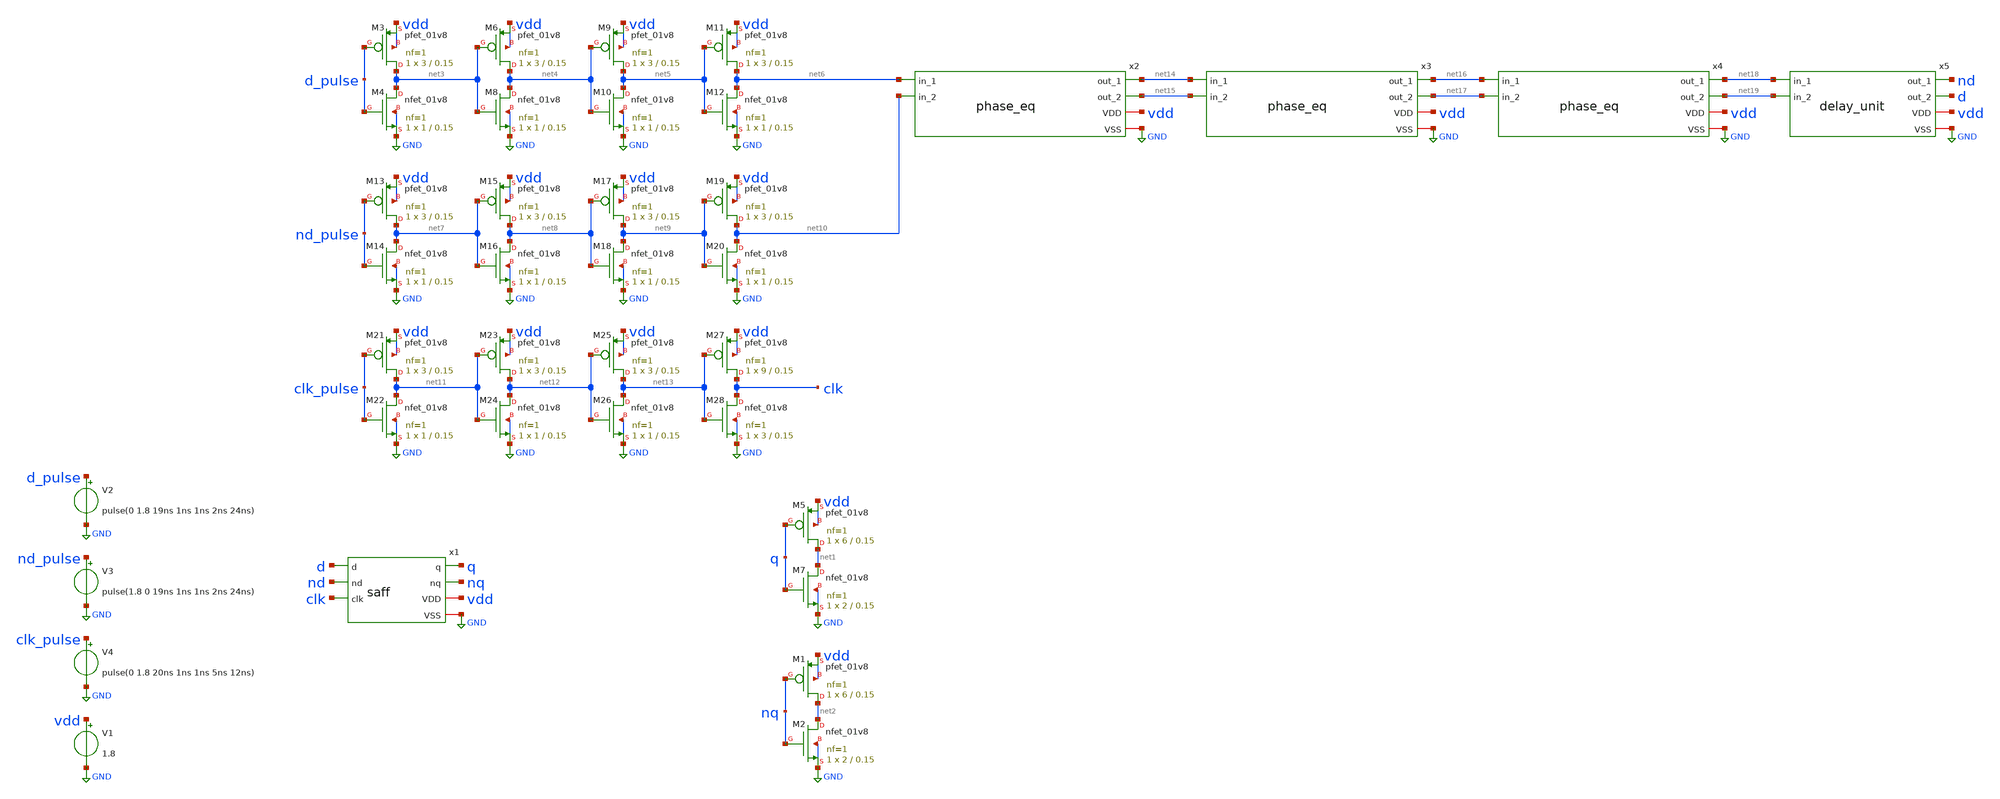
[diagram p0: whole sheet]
** sch_path: xschem/saff_tb.sch
**.subckt saff_tb
x1 d nd clk q nq vdd GND saff
V1 vdd GND 1.8
V2 d_pulse GND pulse(0 1.8 19ns 1ns 1ns 2ns 24ns)
V3 nd_pulse GND pulse(1.8 0 19ns 1ns 1ns 2ns 24ns)
V4 clk_pulse GND pulse(0 1.8 20ns 1ns 1ns 5ns 12ns)
XM5 net1 q vdd vdd sky130_fd_pr__pfet_01v8 L=0.15 W=6 nf=1 ad='int((nf+1)/2) * W/nf * 0.29' as='int((nf+2)/2) * W/nf * 0.29'
+ pd='2*int((nf+1)/2) * (W/nf + 0.29)' ps='2*int((nf+2)/2) * (W/nf + 0.29)' nrd='0.29 / W' nrs='0.29 / W'
+ sa=0 sb=0 sd=0 mult=1 m=1
XM7 net1 q GND GND sky130_fd_pr__nfet_01v8 L=0.15 W=2 nf=1 ad='int((nf+1)/2) * W/nf * 0.29' as='int((nf+2)/2) * W/nf * 0.29'
+ pd='2*int((nf+1)/2) * (W/nf + 0.29)' ps='2*int((nf+2)/2) * (W/nf + 0.29)' nrd='0.29 / W' nrs='0.29 / W'
+ sa=0 sb=0 sd=0 mult=1 m=1
XM1 net2 nq vdd vdd sky130_fd_pr__pfet_01v8 L=0.15 W=6 nf=1 ad='int((nf+1)/2) * W/nf * 0.29' as='int((nf+2)/2) * W/nf * 0.29'
+ pd='2*int((nf+1)/2) * (W/nf + 0.29)' ps='2*int((nf+2)/2) * (W/nf + 0.29)' nrd='0.29 / W' nrs='0.29 / W'
+ sa=0 sb=0 sd=0 mult=1 m=1
XM2 net2 nq GND GND sky130_fd_pr__nfet_01v8 L=0.15 W=2 nf=1 ad='int((nf+1)/2) * W/nf * 0.29' as='int((nf+2)/2) * W/nf * 0.29'
+ pd='2*int((nf+1)/2) * (W/nf + 0.29)' ps='2*int((nf+2)/2) * (W/nf + 0.29)' nrd='0.29 / W' nrs='0.29 / W'
+ sa=0 sb=0 sd=0 mult=1 m=1
XM3 net3 d_pulse vdd vdd sky130_fd_pr__pfet_01v8 L=0.15 W=3 nf=1 ad='int((nf+1)/2) * W/nf * 0.29' as='int((nf+2)/2) * W/nf * 0.29'
+ pd='2*int((nf+1)/2) * (W/nf + 0.29)' ps='2*int((nf+2)/2) * (W/nf + 0.29)' nrd='0.29 / W' nrs='0.29 / W'
+ sa=0 sb=0 sd=0 mult=1 m=1
XM4 net3 d_pulse GND GND sky130_fd_pr__nfet_01v8 L=0.15 W=1 nf=1 ad='int((nf+1)/2) * W/nf * 0.29' as='int((nf+2)/2) * W/nf * 0.29'
+ pd='2*int((nf+1)/2) * (W/nf + 0.29)' ps='2*int((nf+2)/2) * (W/nf + 0.29)' nrd='0.29 / W' nrs='0.29 / W'
+ sa=0 sb=0 sd=0 mult=1 m=1
XM6 net4 net3 vdd vdd sky130_fd_pr__pfet_01v8 L=0.15 W=3 nf=1 ad='int((nf+1)/2) * W/nf * 0.29' as='int((nf+2)/2) * W/nf * 0.29'
+ pd='2*int((nf+1)/2) * (W/nf + 0.29)' ps='2*int((nf+2)/2) * (W/nf + 0.29)' nrd='0.29 / W' nrs='0.29 / W'
+ sa=0 sb=0 sd=0 mult=1 m=1
XM8 net4 net3 GND GND sky130_fd_pr__nfet_01v8 L=0.15 W=1 nf=1 ad='int((nf+1)/2) * W/nf * 0.29' as='int((nf+2)/2) * W/nf * 0.29'
+ pd='2*int((nf+1)/2) * (W/nf + 0.29)' ps='2*int((nf+2)/2) * (W/nf + 0.29)' nrd='0.29 / W' nrs='0.29 / W'
+ sa=0 sb=0 sd=0 mult=1 m=1
XM9 net5 net4 vdd vdd sky130_fd_pr__pfet_01v8 L=0.15 W=3 nf=1 ad='int((nf+1)/2) * W/nf * 0.29' as='int((nf+2)/2) * W/nf * 0.29'
+ pd='2*int((nf+1)/2) * (W/nf + 0.29)' ps='2*int((nf+2)/2) * (W/nf + 0.29)' nrd='0.29 / W' nrs='0.29 / W'
+ sa=0 sb=0 sd=0 mult=1 m=1
XM10 net5 net4 GND GND sky130_fd_pr__nfet_01v8 L=0.15 W=1 nf=1 ad='int((nf+1)/2) * W/nf * 0.29' as='int((nf+2)/2) * W/nf * 0.29'
+ pd='2*int((nf+1)/2) * (W/nf + 0.29)' ps='2*int((nf+2)/2) * (W/nf + 0.29)' nrd='0.29 / W' nrs='0.29 / W'
+ sa=0 sb=0 sd=0 mult=1 m=1
XM11 net6 net5 vdd vdd sky130_fd_pr__pfet_01v8 L=0.15 W=3 nf=1 ad='int((nf+1)/2) * W/nf * 0.29' as='int((nf+2)/2) * W/nf * 0.29'
+ pd='2*int((nf+1)/2) * (W/nf + 0.29)' ps='2*int((nf+2)/2) * (W/nf + 0.29)' nrd='0.29 / W' nrs='0.29 / W'
+ sa=0 sb=0 sd=0 mult=1 m=1
XM12 net6 net5 GND GND sky130_fd_pr__nfet_01v8 L=0.15 W=1 nf=1 ad='int((nf+1)/2) * W/nf * 0.29' as='int((nf+2)/2) * W/nf * 0.29'
+ pd='2*int((nf+1)/2) * (W/nf + 0.29)' ps='2*int((nf+2)/2) * (W/nf + 0.29)' nrd='0.29 / W' nrs='0.29 / W'
+ sa=0 sb=0 sd=0 mult=1 m=1
XM13 net7 nd_pulse vdd vdd sky130_fd_pr__pfet_01v8 L=0.15 W=3 nf=1 ad='int((nf+1)/2) * W/nf * 0.29' as='int((nf+2)/2) * W/nf * 0.29'
+ pd='2*int((nf+1)/2) * (W/nf + 0.29)' ps='2*int((nf+2)/2) * (W/nf + 0.29)' nrd='0.29 / W' nrs='0.29 / W'
+ sa=0 sb=0 sd=0 mult=1 m=1
XM14 net7 nd_pulse GND GND sky130_fd_pr__nfet_01v8 L=0.15 W=1 nf=1 ad='int((nf+1)/2) * W/nf * 0.29' as='int((nf+2)/2) * W/nf * 0.29'
+ pd='2*int((nf+1)/2) * (W/nf + 0.29)' ps='2*int((nf+2)/2) * (W/nf + 0.29)' nrd='0.29 / W' nrs='0.29 / W'
+ sa=0 sb=0 sd=0 mult=1 m=1
XM15 net8 net7 vdd vdd sky130_fd_pr__pfet_01v8 L=0.15 W=3 nf=1 ad='int((nf+1)/2) * W/nf * 0.29' as='int((nf+2)/2) * W/nf * 0.29'
+ pd='2*int((nf+1)/2) * (W/nf + 0.29)' ps='2*int((nf+2)/2) * (W/nf + 0.29)' nrd='0.29 / W' nrs='0.29 / W'
+ sa=0 sb=0 sd=0 mult=1 m=1
XM16 net8 net7 GND GND sky130_fd_pr__nfet_01v8 L=0.15 W=1 nf=1 ad='int((nf+1)/2) * W/nf * 0.29' as='int((nf+2)/2) * W/nf * 0.29'
+ pd='2*int((nf+1)/2) * (W/nf + 0.29)' ps='2*int((nf+2)/2) * (W/nf + 0.29)' nrd='0.29 / W' nrs='0.29 / W'
+ sa=0 sb=0 sd=0 mult=1 m=1
XM17 net9 net8 vdd vdd sky130_fd_pr__pfet_01v8 L=0.15 W=3 nf=1 ad='int((nf+1)/2) * W/nf * 0.29' as='int((nf+2)/2) * W/nf * 0.29'
+ pd='2*int((nf+1)/2) * (W/nf + 0.29)' ps='2*int((nf+2)/2) * (W/nf + 0.29)' nrd='0.29 / W' nrs='0.29 / W'
+ sa=0 sb=0 sd=0 mult=1 m=1
XM18 net9 net8 GND GND sky130_fd_pr__nfet_01v8 L=0.15 W=1 nf=1 ad='int((nf+1)/2) * W/nf * 0.29' as='int((nf+2)/2) * W/nf * 0.29'
+ pd='2*int((nf+1)/2) * (W/nf + 0.29)' ps='2*int((nf+2)/2) * (W/nf + 0.29)' nrd='0.29 / W' nrs='0.29 / W'
+ sa=0 sb=0 sd=0 mult=1 m=1
XM19 net10 net9 vdd vdd sky130_fd_pr__pfet_01v8 L=0.15 W=3 nf=1 ad='int((nf+1)/2) * W/nf * 0.29' as='int((nf+2)/2) * W/nf * 0.29'
+ pd='2*int((nf+1)/2) * (W/nf + 0.29)' ps='2*int((nf+2)/2) * (W/nf + 0.29)' nrd='0.29 / W' nrs='0.29 / W'
+ sa=0 sb=0 sd=0 mult=1 m=1
XM20 net10 net9 GND GND sky130_fd_pr__nfet_01v8 L=0.15 W=1 nf=1 ad='int((nf+1)/2) * W/nf * 0.29' as='int((nf+2)/2) * W/nf * 0.29'
+ pd='2*int((nf+1)/2) * (W/nf + 0.29)' ps='2*int((nf+2)/2) * (W/nf + 0.29)' nrd='0.29 / W' nrs='0.29 / W'
+ sa=0 sb=0 sd=0 mult=1 m=1
XM21 net11 clk_pulse vdd vdd sky130_fd_pr__pfet_01v8 L=0.15 W=3 nf=1 ad='int((nf+1)/2) * W/nf * 0.29'
+ as='int((nf+2)/2) * W/nf * 0.29' pd='2*int((nf+1)/2) * (W/nf + 0.29)' ps='2*int((nf+2)/2) * (W/nf + 0.29)'
+ nrd='0.29 / W' nrs='0.29 / W' sa=0 sb=0 sd=0 mult=1 m=1
XM22 net11 clk_pulse GND GND sky130_fd_pr__nfet_01v8 L=0.15 W=1 nf=1 ad='int((nf+1)/2) * W/nf * 0.29'
+ as='int((nf+2)/2) * W/nf * 0.29' pd='2*int((nf+1)/2) * (W/nf + 0.29)' ps='2*int((nf+2)/2) * (W/nf + 0.29)'
+ nrd='0.29 / W' nrs='0.29 / W' sa=0 sb=0 sd=0 mult=1 m=1
XM23 net12 net11 vdd vdd sky130_fd_pr__pfet_01v8 L=0.15 W=3 nf=1 ad='int((nf+1)/2) * W/nf * 0.29' as='int((nf+2)/2) * W/nf * 0.29'
+ pd='2*int((nf+1)/2) * (W/nf + 0.29)' ps='2*int((nf+2)/2) * (W/nf + 0.29)' nrd='0.29 / W' nrs='0.29 / W'
+ sa=0 sb=0 sd=0 mult=1 m=1
XM24 net12 net11 GND GND sky130_fd_pr__nfet_01v8 L=0.15 W=1 nf=1 ad='int((nf+1)/2) * W/nf * 0.29' as='int((nf+2)/2) * W/nf * 0.29'
+ pd='2*int((nf+1)/2) * (W/nf + 0.29)' ps='2*int((nf+2)/2) * (W/nf + 0.29)' nrd='0.29 / W' nrs='0.29 / W'
+ sa=0 sb=0 sd=0 mult=1 m=1
XM25 net13 net12 vdd vdd sky130_fd_pr__pfet_01v8 L=0.15 W=3 nf=1 ad='int((nf+1)/2) * W/nf * 0.29' as='int((nf+2)/2) * W/nf * 0.29'
+ pd='2*int((nf+1)/2) * (W/nf + 0.29)' ps='2*int((nf+2)/2) * (W/nf + 0.29)' nrd='0.29 / W' nrs='0.29 / W'
+ sa=0 sb=0 sd=0 mult=1 m=1
XM26 net13 net12 GND GND sky130_fd_pr__nfet_01v8 L=0.15 W=1 nf=1 ad='int((nf+1)/2) * W/nf * 0.29' as='int((nf+2)/2) * W/nf * 0.29'
+ pd='2*int((nf+1)/2) * (W/nf + 0.29)' ps='2*int((nf+2)/2) * (W/nf + 0.29)' nrd='0.29 / W' nrs='0.29 / W'
+ sa=0 sb=0 sd=0 mult=1 m=1
XM27 clk net13 vdd vdd sky130_fd_pr__pfet_01v8 L=0.15 W=9 nf=1 ad='int((nf+1)/2) * W/nf * 0.29' as='int((nf+2)/2) * W/nf * 0.29'
+ pd='2*int((nf+1)/2) * (W/nf + 0.29)' ps='2*int((nf+2)/2) * (W/nf + 0.29)' nrd='0.29 / W' nrs='0.29 / W'
+ sa=0 sb=0 sd=0 mult=1 m=1
XM28 clk net13 GND GND sky130_fd_pr__nfet_01v8 L=0.15 W=3 nf=1 ad='int((nf+1)/2) * W/nf * 0.29' as='int((nf+2)/2) * W/nf * 0.29'
+ pd='2*int((nf+1)/2) * (W/nf + 0.29)' ps='2*int((nf+2)/2) * (W/nf + 0.29)' nrd='0.29 / W' nrs='0.29 / W'
+ sa=0 sb=0 sd=0 mult=1 m=1
x2 net14 net6 net15 net10 vdd GND phase_eq
x3 net16 net14 net17 net15 vdd GND phase_eq
x4 net18 net16 net19 net17 vdd GND phase_eq
x5 nd net18 net19 vdd d GND delay_unit
**** begin user architecture code

** opencircuitdesign pdks install
.lib $::SKYWATER_MODELS/sky130.lib.spice tt





.tran 0.001n 50n
.save v(d) v(nd) v(clk) v(q) v(nq) v(x1.left_latch_1) v(x1.right_latch_1) v(x1.left_latch_2) v(x1.right_latch_2)

.control
run
set wr_vecnames
wrdata saff_tb.txt v(d) v(nd) v(clk) v(q) v(nq) v(x1.left_latch_1) v(x1.right_latch_1)
+ v(x1.left_latch_2) v(x1.right_latch_2)
.endc


**** end user architecture code
**.ends

* expanding   symbol:  saff.sym # of pins=7
** sym_path: xschem/saff.sym
** sch_path: xschem/saff.sch
.subckt saff d nd clk q nq VDD VSS
*.iopin VDD
*.ipin d
*.opin q
*.iopin VSS
*.ipin nd
*.ipin clk
*.opin nq
XM2 net3 q VSS VSS sky130_fd_pr__nfet_01v8 L=0.15 W=1 nf=1 ad='int((nf+1)/2) * W/nf * 0.29' as='int((nf+2)/2) * W/nf * 0.29'
+ pd='2*int((nf+1)/2) * (W/nf + 0.29)' ps='2*int((nf+2)/2) * (W/nf + 0.29)' nrd='0.29 / W' nrs='0.29 / W'
+ sa=0 sb=0 sd=0 mult=1 m=1
XM3 left_latch_1 clk VDD VDD sky130_fd_pr__pfet_01v8 L=0.15 W=3 nf=1 ad='int((nf+1)/2) * W/nf * 0.29'
+ as='int((nf+2)/2) * W/nf * 0.29' pd='2*int((nf+1)/2) * (W/nf + 0.29)' ps='2*int((nf+2)/2) * (W/nf + 0.29)'
+ nrd='0.29 / W' nrs='0.29 / W' sa=0 sb=0 sd=0 mult=1 m=1
XM4 right_latch_1 clk VDD VDD sky130_fd_pr__pfet_01v8 L=0.15 W=3 nf=1 ad='int((nf+1)/2) * W/nf * 0.29'
+ as='int((nf+2)/2) * W/nf * 0.29' pd='2*int((nf+1)/2) * (W/nf + 0.29)' ps='2*int((nf+2)/2) * (W/nf + 0.29)'
+ nrd='0.29 / W' nrs='0.29 / W' sa=0 sb=0 sd=0 mult=1 m=1
XM5 right_latch_1 left_latch_1 VDD VDD sky130_fd_pr__pfet_01v8 L=0.15 W=3 nf=1 ad='int((nf+1)/2) * W/nf * 0.29'
+ as='int((nf+2)/2) * W/nf * 0.29' pd='2*int((nf+1)/2) * (W/nf + 0.29)' ps='2*int((nf+2)/2) * (W/nf + 0.29)'
+ nrd='0.29 / W' nrs='0.29 / W' sa=0 sb=0 sd=0 mult=1 m=1
XM6 left_latch_1 right_latch_1 VDD VDD sky130_fd_pr__pfet_01v8 L=0.15 W=3 nf=1 ad='int((nf+1)/2) * W/nf * 0.29'
+ as='int((nf+2)/2) * W/nf * 0.29' pd='2*int((nf+1)/2) * (W/nf + 0.29)' ps='2*int((nf+2)/2) * (W/nf + 0.29)'
+ nrd='0.29 / W' nrs='0.29 / W' sa=0 sb=0 sd=0 mult=1 m=1
XM7 right_latch_1 left_latch_1 net7 VSS sky130_fd_pr__nfet_01v8 L=0.15 W=6 nf=1 ad='int((nf+1)/2) * W/nf * 0.29'
+ as='int((nf+2)/2) * W/nf * 0.29' pd='2*int((nf+1)/2) * (W/nf + 0.29)' ps='2*int((nf+2)/2) * (W/nf + 0.29)'
+ nrd='0.29 / W' nrs='0.29 / W' sa=0 sb=0 sd=0 mult=1 m=1
XM8 left_latch_1 right_latch_1 net5 VSS sky130_fd_pr__nfet_01v8 L=0.15 W=6 nf=1 ad='int((nf+1)/2) * W/nf * 0.29'
+ as='int((nf+2)/2) * W/nf * 0.29' pd='2*int((nf+1)/2) * (W/nf + 0.29)' ps='2*int((nf+2)/2) * (W/nf + 0.29)'
+ nrd='0.29 / W' nrs='0.29 / W' sa=0 sb=0 sd=0 mult=1 m=1
XM9 net6 clk VSS VSS sky130_fd_pr__nfet_01v8 L=0.15 W=15 nf=1 ad='int((nf+1)/2) * W/nf * 0.29' as='int((nf+2)/2) * W/nf * 0.29'
+ pd='2*int((nf+1)/2) * (W/nf + 0.29)' ps='2*int((nf+2)/2) * (W/nf + 0.29)' nrd='0.29 / W' nrs='0.29 / W'
+ sa=0 sb=0 sd=0 mult=1 m=1
XM10 net7 nd net6 VSS sky130_fd_pr__nfet_01v8 L=0.15 W=12 nf=1 ad='int((nf+1)/2) * W/nf * 0.29' as='int((nf+2)/2) * W/nf * 0.29'
+ pd='2*int((nf+1)/2) * (W/nf + 0.29)' ps='2*int((nf+2)/2) * (W/nf + 0.29)' nrd='0.29 / W' nrs='0.29 / W'
+ sa=0 sb=0 sd=0 mult=1 m=1
XM11 net5 d net6 VSS sky130_fd_pr__nfet_01v8 L=0.15 W=12 nf=1 ad='int((nf+1)/2) * W/nf * 0.29' as='int((nf+2)/2) * W/nf * 0.29'
+ pd='2*int((nf+1)/2) * (W/nf + 0.29)' ps='2*int((nf+2)/2) * (W/nf + 0.29)' nrd='0.29 / W' nrs='0.29 / W'
+ sa=0 sb=0 sd=0 mult=1 m=1
XM12 right_latch_2 left_latch_1 VDD VDD sky130_fd_pr__pfet_01v8 L=0.15 W=6 nf=1 ad='int((nf+1)/2) * W/nf * 0.29'
+ as='int((nf+2)/2) * W/nf * 0.29' pd='2*int((nf+1)/2) * (W/nf + 0.29)' ps='2*int((nf+2)/2) * (W/nf + 0.29)'
+ nrd='0.29 / W' nrs='0.29 / W' sa=0 sb=0 sd=0 mult=1 m=1
XM13 right_latch_2 left_latch_1 VSS VSS sky130_fd_pr__nfet_01v8 L=0.15 W=2 nf=1 ad='int((nf+1)/2) * W/nf * 0.29'
+ as='int((nf+2)/2) * W/nf * 0.29' pd='2*int((nf+1)/2) * (W/nf + 0.29)' ps='2*int((nf+2)/2) * (W/nf + 0.29)'
+ nrd='0.29 / W' nrs='0.29 / W' sa=0 sb=0 sd=0 mult=1 m=1
XM14 left_latch_2 right_latch_1 VDD VDD sky130_fd_pr__pfet_01v8 L=0.15 W=6 nf=1 ad='int((nf+1)/2) * W/nf * 0.29'
+ as='int((nf+2)/2) * W/nf * 0.29' pd='2*int((nf+1)/2) * (W/nf + 0.29)' ps='2*int((nf+2)/2) * (W/nf + 0.29)'
+ nrd='0.29 / W' nrs='0.29 / W' sa=0 sb=0 sd=0 mult=1 m=1
XM15 left_latch_2 right_latch_1 VSS VSS sky130_fd_pr__nfet_01v8 L=0.15 W=2 nf=1 ad='int((nf+1)/2) * W/nf * 0.29'
+ as='int((nf+2)/2) * W/nf * 0.29' pd='2*int((nf+1)/2) * (W/nf + 0.29)' ps='2*int((nf+2)/2) * (W/nf + 0.29)'
+ nrd='0.29 / W' nrs='0.29 / W' sa=0 sb=0 sd=0 mult=1 m=1
XM16 q left_latch_1 VDD VDD sky130_fd_pr__pfet_01v8 L=0.15 W=3 nf=1 ad='int((nf+1)/2) * W/nf * 0.29'
+ as='int((nf+2)/2) * W/nf * 0.29' pd='2*int((nf+1)/2) * (W/nf + 0.29)' ps='2*int((nf+2)/2) * (W/nf + 0.29)'
+ nrd='0.29 / W' nrs='0.29 / W' sa=0 sb=0 sd=0 mult=1 m=1
XM17 q left_latch_2 VSS VSS sky130_fd_pr__nfet_01v8 L=0.15 W=1 nf=1 ad='int((nf+1)/2) * W/nf * 0.29'
+ as='int((nf+2)/2) * W/nf * 0.29' pd='2*int((nf+1)/2) * (W/nf + 0.29)' ps='2*int((nf+2)/2) * (W/nf + 0.29)'
+ nrd='0.29 / W' nrs='0.29 / W' sa=0 sb=0 sd=0 mult=1 m=1
XM18 nq right_latch_1 VDD VDD sky130_fd_pr__pfet_01v8 L=0.15 W=3 nf=1 ad='int((nf+1)/2) * W/nf * 0.29'
+ as='int((nf+2)/2) * W/nf * 0.29' pd='2*int((nf+1)/2) * (W/nf + 0.29)' ps='2*int((nf+2)/2) * (W/nf + 0.29)'
+ nrd='0.29 / W' nrs='0.29 / W' sa=0 sb=0 sd=0 mult=1 m=1
XM19 nq right_latch_2 VSS VSS sky130_fd_pr__nfet_01v8 L=0.15 W=1 nf=1 ad='int((nf+1)/2) * W/nf * 0.29'
+ as='int((nf+2)/2) * W/nf * 0.29' pd='2*int((nf+1)/2) * (W/nf + 0.29)' ps='2*int((nf+2)/2) * (W/nf + 0.29)'
+ nrd='0.29 / W' nrs='0.29 / W' sa=0 sb=0 sd=0 mult=1 m=1
XM20 net2 q VDD VDD sky130_fd_pr__pfet_01v8 L=0.15 W=3 nf=1 ad='int((nf+1)/2) * W/nf * 0.29' as='int((nf+2)/2) * W/nf * 0.29'
+ pd='2*int((nf+1)/2) * (W/nf + 0.29)' ps='2*int((nf+2)/2) * (W/nf + 0.29)' nrd='0.29 / W' nrs='0.29 / W'
+ sa=0 sb=0 sd=0 mult=1 m=1
XM21 nq right_latch_2 net2 VDD sky130_fd_pr__pfet_01v8 L=0.15 W=3 nf=1 ad='int((nf+1)/2) * W/nf * 0.29'
+ as='int((nf+2)/2) * W/nf * 0.29' pd='2*int((nf+1)/2) * (W/nf + 0.29)' ps='2*int((nf+2)/2) * (W/nf + 0.29)'
+ nrd='0.29 / W' nrs='0.29 / W' sa=0 sb=0 sd=0 mult=1 m=1
XM22 q left_latch_2 net1 VDD sky130_fd_pr__pfet_01v8 L=0.15 W=3 nf=1 ad='int((nf+1)/2) * W/nf * 0.29'
+ as='int((nf+2)/2) * W/nf * 0.29' pd='2*int((nf+1)/2) * (W/nf + 0.29)' ps='2*int((nf+2)/2) * (W/nf + 0.29)'
+ nrd='0.29 / W' nrs='0.29 / W' sa=0 sb=0 sd=0 mult=1 m=1
XM23 net1 nq VDD VDD sky130_fd_pr__pfet_01v8 L=0.15 W=3 nf=1 ad='int((nf+1)/2) * W/nf * 0.29' as='int((nf+2)/2) * W/nf * 0.29'
+ pd='2*int((nf+1)/2) * (W/nf + 0.29)' ps='2*int((nf+2)/2) * (W/nf + 0.29)' nrd='0.29 / W' nrs='0.29 / W'
+ sa=0 sb=0 sd=0 mult=1 m=1
XM24 q left_latch_1 net4 VSS sky130_fd_pr__nfet_01v8 L=0.15 W=1 nf=1 ad='int((nf+1)/2) * W/nf * 0.29'
+ as='int((nf+2)/2) * W/nf * 0.29' pd='2*int((nf+1)/2) * (W/nf + 0.29)' ps='2*int((nf+2)/2) * (W/nf + 0.29)'
+ nrd='0.29 / W' nrs='0.29 / W' sa=0 sb=0 sd=0 mult=1 m=1
XM25 nq right_latch_1 net3 VSS sky130_fd_pr__nfet_01v8 L=0.15 W=1 nf=1 ad='int((nf+1)/2) * W/nf * 0.29'
+ as='int((nf+2)/2) * W/nf * 0.29' pd='2*int((nf+1)/2) * (W/nf + 0.29)' ps='2*int((nf+2)/2) * (W/nf + 0.29)'
+ nrd='0.29 / W' nrs='0.29 / W' sa=0 sb=0 sd=0 mult=1 m=1
XM26 net4 nq VSS VSS sky130_fd_pr__nfet_01v8 L=0.15 W=1 nf=1 ad='int((nf+1)/2) * W/nf * 0.29' as='int((nf+2)/2) * W/nf * 0.29'
+ pd='2*int((nf+1)/2) * (W/nf + 0.29)' ps='2*int((nf+2)/2) * (W/nf + 0.29)' nrd='0.29 / W' nrs='0.29 / W'
+ sa=0 sb=0 sd=0 mult=1 m=1
.ends


* expanding   symbol:  phase_eq.sym # of pins=6
** sym_path: xschem/phase_eq.sym
** sch_path: xschem/phase_eq.sch
.subckt phase_eq out_1 in_1 out_2 in_2 VDD VSS
*.iopin VDD
*.ipin in_1
*.opin out_1
*.iopin VSS
*.ipin in_2
*.opin out_2
XM5 out_1 in_1 VDD VDD sky130_fd_pr__pfet_01v8 L=0.15 W=9 nf=1 ad='int((nf+1)/2) * W/nf * 0.29' as='int((nf+2)/2) * W/nf * 0.29'
+ pd='2*int((nf+1)/2) * (W/nf + 0.29)' ps='2*int((nf+2)/2) * (W/nf + 0.29)' nrd='0.29 / W' nrs='0.29 / W'
+ sa=0 sb=0 sd=0 mult=1 m=1
XM7 out_1 in_1 VSS VSS sky130_fd_pr__nfet_01v8 L=0.15 W=3 nf=1 ad='int((nf+1)/2) * W/nf * 0.29' as='int((nf+2)/2) * W/nf * 0.29'
+ pd='2*int((nf+1)/2) * (W/nf + 0.29)' ps='2*int((nf+2)/2) * (W/nf + 0.29)' nrd='0.29 / W' nrs='0.29 / W'
+ sa=0 sb=0 sd=0 mult=1 m=1
XM1 out_2 in_2 VDD VDD sky130_fd_pr__pfet_01v8 L=0.15 W=9 nf=1 ad='int((nf+1)/2) * W/nf * 0.29' as='int((nf+2)/2) * W/nf * 0.29'
+ pd='2*int((nf+1)/2) * (W/nf + 0.29)' ps='2*int((nf+2)/2) * (W/nf + 0.29)' nrd='0.29 / W' nrs='0.29 / W'
+ sa=0 sb=0 sd=0 mult=1 m=1
XM2 out_2 in_2 VSS VSS sky130_fd_pr__nfet_01v8 L=0.15 W=3 nf=1 ad='int((nf+1)/2) * W/nf * 0.29' as='int((nf+2)/2) * W/nf * 0.29'
+ pd='2*int((nf+1)/2) * (W/nf + 0.29)' ps='2*int((nf+2)/2) * (W/nf + 0.29)' nrd='0.29 / W' nrs='0.29 / W'
+ sa=0 sb=0 sd=0 mult=1 m=1
XM3 in_1 in_2 VDD VDD sky130_fd_pr__pfet_01v8 L=0.15 W=3 nf=1 ad='int((nf+1)/2) * W/nf * 0.29' as='int((nf+2)/2) * W/nf * 0.29'
+ pd='2*int((nf+1)/2) * (W/nf + 0.29)' ps='2*int((nf+2)/2) * (W/nf + 0.29)' nrd='0.29 / W' nrs='0.29 / W'
+ sa=0 sb=0 sd=0 mult=1 m=1
XM4 in_1 in_2 VSS VSS sky130_fd_pr__nfet_01v8 L=0.15 W=1 nf=1 ad='int((nf+1)/2) * W/nf * 0.29' as='int((nf+2)/2) * W/nf * 0.29'
+ pd='2*int((nf+1)/2) * (W/nf + 0.29)' ps='2*int((nf+2)/2) * (W/nf + 0.29)' nrd='0.29 / W' nrs='0.29 / W'
+ sa=0 sb=0 sd=0 mult=1 m=1
XM6 in_2 in_1 VDD VDD sky130_fd_pr__pfet_01v8 L=0.15 W=3 nf=1 ad='int((nf+1)/2) * W/nf * 0.29' as='int((nf+2)/2) * W/nf * 0.29'
+ pd='2*int((nf+1)/2) * (W/nf + 0.29)' ps='2*int((nf+2)/2) * (W/nf + 0.29)' nrd='0.29 / W' nrs='0.29 / W'
+ sa=0 sb=0 sd=0 mult=1 m=1
XM8 in_2 in_1 VSS VSS sky130_fd_pr__nfet_01v8 L=0.15 W=1 nf=1 ad='int((nf+1)/2) * W/nf * 0.29' as='int((nf+2)/2) * W/nf * 0.29'
+ pd='2*int((nf+1)/2) * (W/nf + 0.29)' ps='2*int((nf+2)/2) * (W/nf + 0.29)' nrd='0.29 / W' nrs='0.29 / W'
+ sa=0 sb=0 sd=0 mult=1 m=1
.ends


* expanding   symbol:  delay_unit.sym # of pins=6
** sym_path: xschem/delay_unit.sym
** sch_path: xschem/delay_unit.sch
.subckt delay_unit out_1 in_1 in_2 VDD out_2 VSS
*.iopin VDD
*.ipin in_1
*.opin out_1
*.iopin VSS
*.ipin in_2
*.opin out_2
XM5 out_2 in_1 VDD VDD sky130_fd_pr__pfet_01v8 L=0.15 W=9 nf=1 ad='int((nf+1)/2) * W/nf * 0.29' as='int((nf+2)/2) * W/nf * 0.29'
+ pd='2*int((nf+1)/2) * (W/nf + 0.29)' ps='2*int((nf+2)/2) * (W/nf + 0.29)' nrd='0.29 / W' nrs='0.29 / W'
+ sa=0 sb=0 sd=0 mult=1 m=1
XM7 out_2 in_1 VSS VSS sky130_fd_pr__nfet_01v8 L=0.15 W=3 nf=1 ad='int((nf+1)/2) * W/nf * 0.29' as='int((nf+2)/2) * W/nf * 0.29'
+ pd='2*int((nf+1)/2) * (W/nf + 0.29)' ps='2*int((nf+2)/2) * (W/nf + 0.29)' nrd='0.29 / W' nrs='0.29 / W'
+ sa=0 sb=0 sd=0 mult=1 m=1
XM1 out_1 in_2 VDD VDD sky130_fd_pr__pfet_01v8 L=0.15 W=9 nf=1 ad='int((nf+1)/2) * W/nf * 0.29' as='int((nf+2)/2) * W/nf * 0.29'
+ pd='2*int((nf+1)/2) * (W/nf + 0.29)' ps='2*int((nf+2)/2) * (W/nf + 0.29)' nrd='0.29 / W' nrs='0.29 / W'
+ sa=0 sb=0 sd=0 mult=1 m=1
XM2 out_1 in_2 VSS VSS sky130_fd_pr__nfet_01v8 L=0.15 W=3 nf=1 ad='int((nf+1)/2) * W/nf * 0.29' as='int((nf+2)/2) * W/nf * 0.29'
+ pd='2*int((nf+1)/2) * (W/nf + 0.29)' ps='2*int((nf+2)/2) * (W/nf + 0.29)' nrd='0.29 / W' nrs='0.29 / W'
+ sa=0 sb=0 sd=0 mult=1 m=1
XM3 in_1 in_2 VDD VDD sky130_fd_pr__pfet_01v8 L=0.15 W=3 nf=1 ad='int((nf+1)/2) * W/nf * 0.29' as='int((nf+2)/2) * W/nf * 0.29'
+ pd='2*int((nf+1)/2) * (W/nf + 0.29)' ps='2*int((nf+2)/2) * (W/nf + 0.29)' nrd='0.29 / W' nrs='0.29 / W'
+ sa=0 sb=0 sd=0 mult=1 m=1
XM4 in_1 in_2 VSS VSS sky130_fd_pr__nfet_01v8 L=0.15 W=1 nf=1 ad='int((nf+1)/2) * W/nf * 0.29' as='int((nf+2)/2) * W/nf * 0.29'
+ pd='2*int((nf+1)/2) * (W/nf + 0.29)' ps='2*int((nf+2)/2) * (W/nf + 0.29)' nrd='0.29 / W' nrs='0.29 / W'
+ sa=0 sb=0 sd=0 mult=1 m=1
XM6 in_2 in_1 VDD VDD sky130_fd_pr__pfet_01v8 L=0.15 W=3 nf=1 ad='int((nf+1)/2) * W/nf * 0.29' as='int((nf+2)/2) * W/nf * 0.29'
+ pd='2*int((nf+1)/2) * (W/nf + 0.29)' ps='2*int((nf+2)/2) * (W/nf + 0.29)' nrd='0.29 / W' nrs='0.29 / W'
+ sa=0 sb=0 sd=0 mult=1 m=1
XM8 in_2 in_1 VSS VSS sky130_fd_pr__nfet_01v8 L=0.15 W=1 nf=1 ad='int((nf+1)/2) * W/nf * 0.29' as='int((nf+2)/2) * W/nf * 0.29'
+ pd='2*int((nf+1)/2) * (W/nf + 0.29)' ps='2*int((nf+2)/2) * (W/nf + 0.29)' nrd='0.29 / W' nrs='0.29 / W'
+ sa=0 sb=0 sd=0 mult=1 m=1
.ends

.GLOBAL GND
.end
